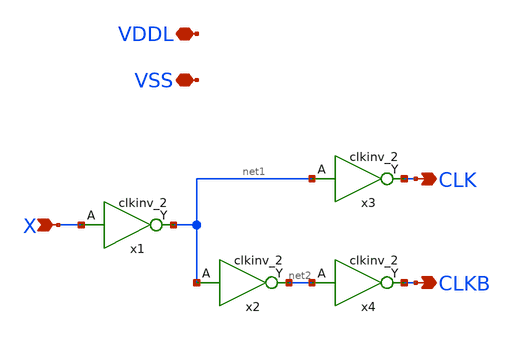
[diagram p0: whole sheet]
** sch_path: xschem/clock_3v3/phase_splitter.sch
**.subckt phase_splitter X CLK CLKB VDDL VSS
*.ipin X
*.opin CLK
*.opin CLKB
*.iopin VDDL
*.iopin VSS
x2 net1 VSS VSS VDDL VDDL net2 sky130_fd_sc_hd__clkinv_2
x1 X VSS VSS VDDL VDDL net1 sky130_fd_sc_hd__clkinv_2
x3 net1 VSS VSS VDDL VDDL CLK sky130_fd_sc_hd__clkinv_2
x4 net2 VSS VSS VDDL VDDL CLKB sky130_fd_sc_hd__clkinv_2
**.ends
.end
